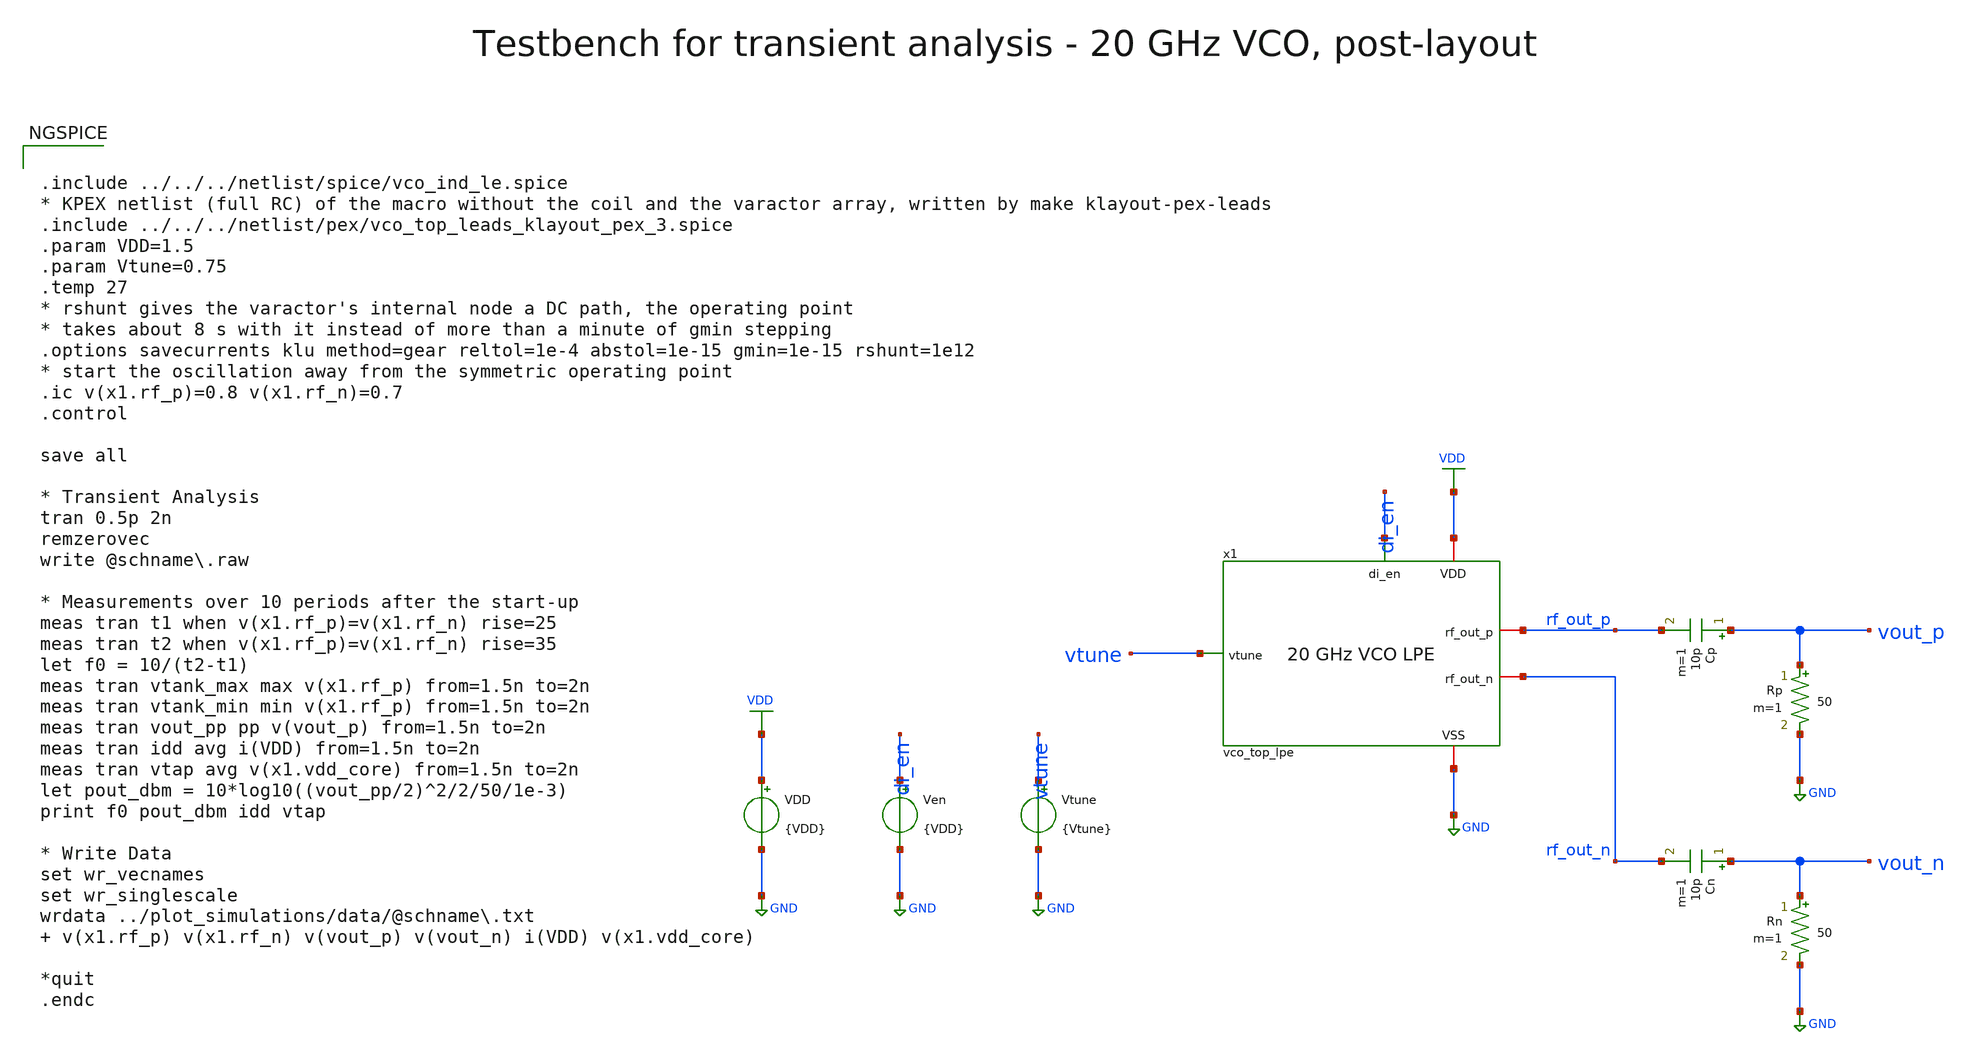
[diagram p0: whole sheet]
** sch_path: macros/vco/testbenches/xschem/vco_top_tb_tran_lpe.sch
**.subckt vco_top_tb_tran_lpe
x1 di_en VDD GND vtune rf_out_p rf_out_n vco_top_lpe
Cp vout_p rf_out_p 10p m=1
Rp vout_p GND 50 m=1
Cn vout_n rf_out_n 10p m=1
Rn vout_n GND 50 m=1
VDD VDD GND {VDD}
Ven di_en GND {VDD}
Vtune vtune GND {Vtune}
**** begin user architecture code


.include ../../../netlist/spice/vco_ind_le.spice
* KPEX netlist (full RC) of the macro without the coil and the varactor array, written by make
*+ klayout-pex-leads
.include ../../../netlist/pex/vco_top_leads_klayout_pex_3.spice
.param VDD=1.5
.param Vtune=0.75
.temp 27
* rshunt gives the varactor's internal node a DC path, the operating point
* takes about 8 s with it instead of more than a minute of gmin stepping
.options savecurrents klu method=gear reltol=1e-4 abstol=1e-15 gmin=1e-15 rshunt=1e12
* start the oscillation away from the symmetric operating point
.ic v(x1.rf_p)=0.8 v(x1.rf_n)=0.7
.control

save all

* Transient Analysis
tran 0.5p 2n
remzerovec
write @schname\.raw

* Measurements over 10 periods after the start-up
meas tran t1 when v(x1.rf_p)=v(x1.rf_n) rise=25
meas tran t2 when v(x1.rf_p)=v(x1.rf_n) rise=35
let f0 = 10/(t2-t1)
meas tran vtank_max max v(x1.rf_p) from=1.5n to=2n
meas tran vtank_min min v(x1.rf_p) from=1.5n to=2n
meas tran vout_pp pp v(vout_p) from=1.5n to=2n
meas tran idd avg i(VDD) from=1.5n to=2n
meas tran vtap avg v(x1.vdd_core) from=1.5n to=2n
let pout_dbm = 10*log10((vout_pp/2)^2/2/50/1e-3)
print f0 pout_dbm idd vtap

* Write Data
set wr_vecnames
set wr_singlescale
wrdata ../plot_simulations/data/@schname\.txt  v(x1.rf_p) v(x1.rf_n) v(vout_p) v(vout_n) i(VDD) v(x1.vdd_core)

*quit
.endc



.lib cornerMOSlv.lib mos_tt
.lib cornerMOShv.lib mos_tt
.lib cornerRES.lib res_typ
.lib cornerCAP.lib cap_typ

**** end user architecture code
**.ends

* expanding   symbol:  vco_top_lpe.sym # of pins=6
** sym_path: macros/vco/testbenches/xschem/vco_top_lpe.sym
** sch_path: macros/vco/testbenches/xschem/vco_top_lpe.sch
.subckt vco_top_lpe di_en VDD VSS vtune rf_out_p rf_out_n
*.iopin VDD
*.iopin VSS
*.ipin di_en
*.ipin vtune
*.iopin rf_out_p
*.iopin rf_out_n
xleads di_en vtune VDD VSS rf_out_p rf_out_n rf_p rf_n vdd_core vco_var_rf_p vco_var_rf_n vco_var_VSS vco_top_leads
xind rf_p rf_n vdd_core vco_ind_le
xvar vco_var_rf_p vco_var_rf_n vtune vco_var_VSS vco_var
.ends


* expanding   symbol:  vco_var.sym # of pins=4
** sym_path: macros/vco/schematic/xschem/vco_var.sym
** sch_path: macros/vco/schematic/xschem/vco_var.sch
.subckt vco_var rf_p rf_n vtune VSS
*.ipin vtune
*.iopin rf_p
*.iopin rf_n
*.iopin VSS
XCvar1 rf_p vtune rf_n VSS sg13_hv_svaricap w=3.74u l=0.3u Nx=7 mm_ok=1
XCvar2 rf_p vtune rf_n VSS sg13_hv_svaricap w=3.74u l=0.3u Nx=7 mm_ok=1
XCvar3 rf_p vtune rf_n VSS sg13_hv_svaricap w=3.74u l=0.3u Nx=7 mm_ok=1
.ends

.GLOBAL VDD
.GLOBAL GND
.end
